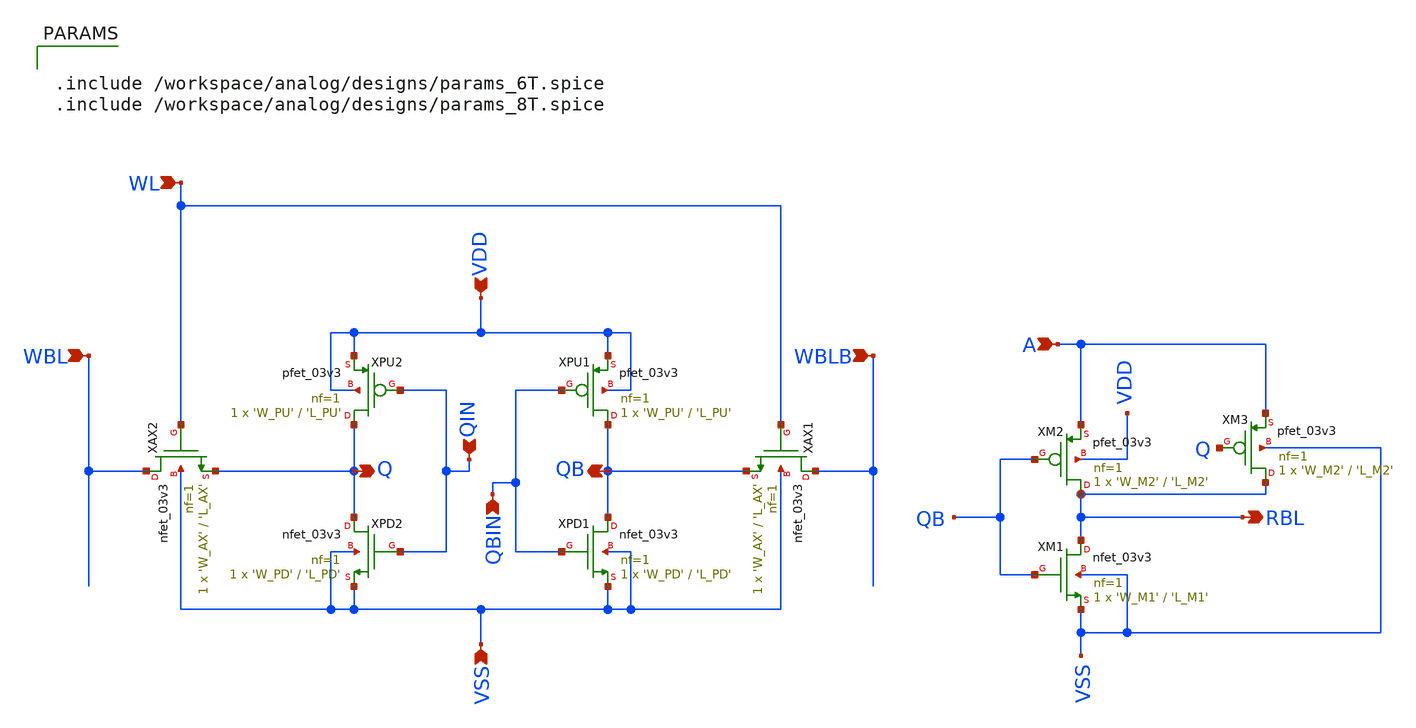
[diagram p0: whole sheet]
** sch_path: analog/designs/8T_03v3.sch
**.subckt 8T_03v3 RBL VSS VDD WL WBL WBLB QBIN QIN Q QB A
*.opin RBL
*.ipin VSS
*.ipin VDD
*.ipin WL
*.ipin WBL
*.ipin WBLB
*.ipin QBIN
*.ipin QIN
*.opin Q
*.opin QB
*.ipin A
XM1 RBL QB VSS VSS nfet_03v3 L='L_M1' W='W_M1' nf=1 ad='int((nf+1)/2) * W/nf * 0.18u' as='int((nf+2)/2) * W/nf * 0.18u'
+ pd='2*int((nf+1)/2) * (W/nf + 0.18u)' ps='2*int((nf+2)/2) * (W/nf + 0.18u)' nrd='0.18u / W' nrs='0.18u / W'
+ sa=0 sb=0 sd=0 m=1
XPD1 QB QBIN VSS VSS nfet_03v3 L='L_PD' W='W_PD' nf=1 ad='int((nf+1)/2) * W/nf * 0.18u' as='int((nf+2)/2) * W/nf * 0.18u'
+ pd='2*int((nf+1)/2) * (W/nf + 0.18u)' ps='2*int((nf+2)/2) * (W/nf + 0.18u)' nrd='0.18u / W' nrs='0.18u / W'
+ sa=0 sb=0 sd=0 m=1
XPU1 QB QBIN VDD VDD pfet_03v3 L='L_PU' W='W_PU' nf=1 ad='int((nf+1)/2) * W/nf * 0.18u' as='int((nf+2)/2) * W/nf * 0.18u'
+ pd='2*int((nf+1)/2) * (W/nf + 0.18u)' ps='2*int((nf+2)/2) * (W/nf + 0.18u)' nrd='0.18u / W' nrs='0.18u / W'
+ sa=0 sb=0 sd=0 m=1
XAX1 WBLB WL QB VSS nfet_03v3 L='L_AX' W='W_AX' nf=1 ad='int((nf+1)/2) * W/nf * 0.18u' as='int((nf+2)/2) * W/nf * 0.18u'
+ pd='2*int((nf+1)/2) * (W/nf + 0.18u)' ps='2*int((nf+2)/2) * (W/nf + 0.18u)' nrd='0.18u / W' nrs='0.18u / W'
+ sa=0 sb=0 sd=0 m=1
XPU2 Q QIN VDD VDD pfet_03v3 L='L_PU' W='W_PU' nf=1 ad='int((nf+1)/2) * W/nf * 0.18u' as='int((nf+2)/2) * W/nf * 0.18u'
+ pd='2*int((nf+1)/2) * (W/nf + 0.18u)' ps='2*int((nf+2)/2) * (W/nf + 0.18u)' nrd='0.18u / W' nrs='0.18u / W'
+ sa=0 sb=0 sd=0 m=1
XPD2 Q QIN VSS VSS nfet_03v3 L='L_PD' W='W_PD' nf=1 ad='int((nf+1)/2) * W/nf * 0.18u' as='int((nf+2)/2) * W/nf * 0.18u'
+ pd='2*int((nf+1)/2) * (W/nf + 0.18u)' ps='2*int((nf+2)/2) * (W/nf + 0.18u)' nrd='0.18u / W' nrs='0.18u / W'
+ sa=0 sb=0 sd=0 m=1
XAX2 WBL WL Q VSS nfet_03v3 L='L_AX' W='W_AX' nf=1 ad='int((nf+1)/2) * W/nf * 0.18u' as='int((nf+2)/2) * W/nf * 0.18u'
+ pd='2*int((nf+1)/2) * (W/nf + 0.18u)' ps='2*int((nf+2)/2) * (W/nf + 0.18u)' nrd='0.18u / W' nrs='0.18u / W'
+ sa=0 sb=0 sd=0 m=1
XM2 RBL QB A VDD pfet_03v3 L='L_M2' W='W_M2' nf=1 ad='int((nf+1)/2) * W/nf * 0.18u' as='int((nf+2)/2) * W/nf * 0.18u'
+ pd='2*int((nf+1)/2) * (W/nf + 0.18u)' ps='2*int((nf+2)/2) * (W/nf + 0.18u)' nrd='0.18u / W' nrs='0.18u / W'
+ sa=0 sb=0 sd=0 m=1
XM3 RBL Q A VSS pfet_03v3 L='L_M2' W='W_M2' nf=1 ad='int((nf+1)/2) * W/nf * 0.18u' as='int((nf+2)/2) * W/nf * 0.18u'
+ pd='2*int((nf+1)/2) * (W/nf + 0.18u)' ps='2*int((nf+2)/2) * (W/nf + 0.18u)' nrd='0.18u / W' nrs='0.18u / W'
+ sa=0 sb=0 sd=0 m=1
**** begin user architecture code

.include /workspace/analog/designs/params_6T.spice
.include /workspace/analog/designs/params_8T.spice

**** end user architecture code
**.ends
.end
